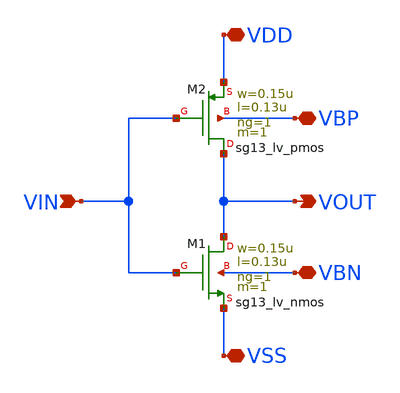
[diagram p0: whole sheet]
** sch_path: CDR4176-main/schematic/xschem/inv_xor/inv_xor.sch
**.subckt inv_xor VDD VSS VOUT VIN VBP VBN
*.iopin VDD
*.iopin VSS
*.opin VOUT
*.ipin VIN
*.iopin VBP
*.iopin VBN
XM2 VOUT VIN VDD VBP sg13_lv_pmos w=0.15u l=0.13u ng=1 m=1 mm_ok=1
XM1 VOUT VIN VSS VBN sg13_lv_nmos w=0.15u l=0.13u ng=1 m=1 mm_ok=1
**.ends
.end
